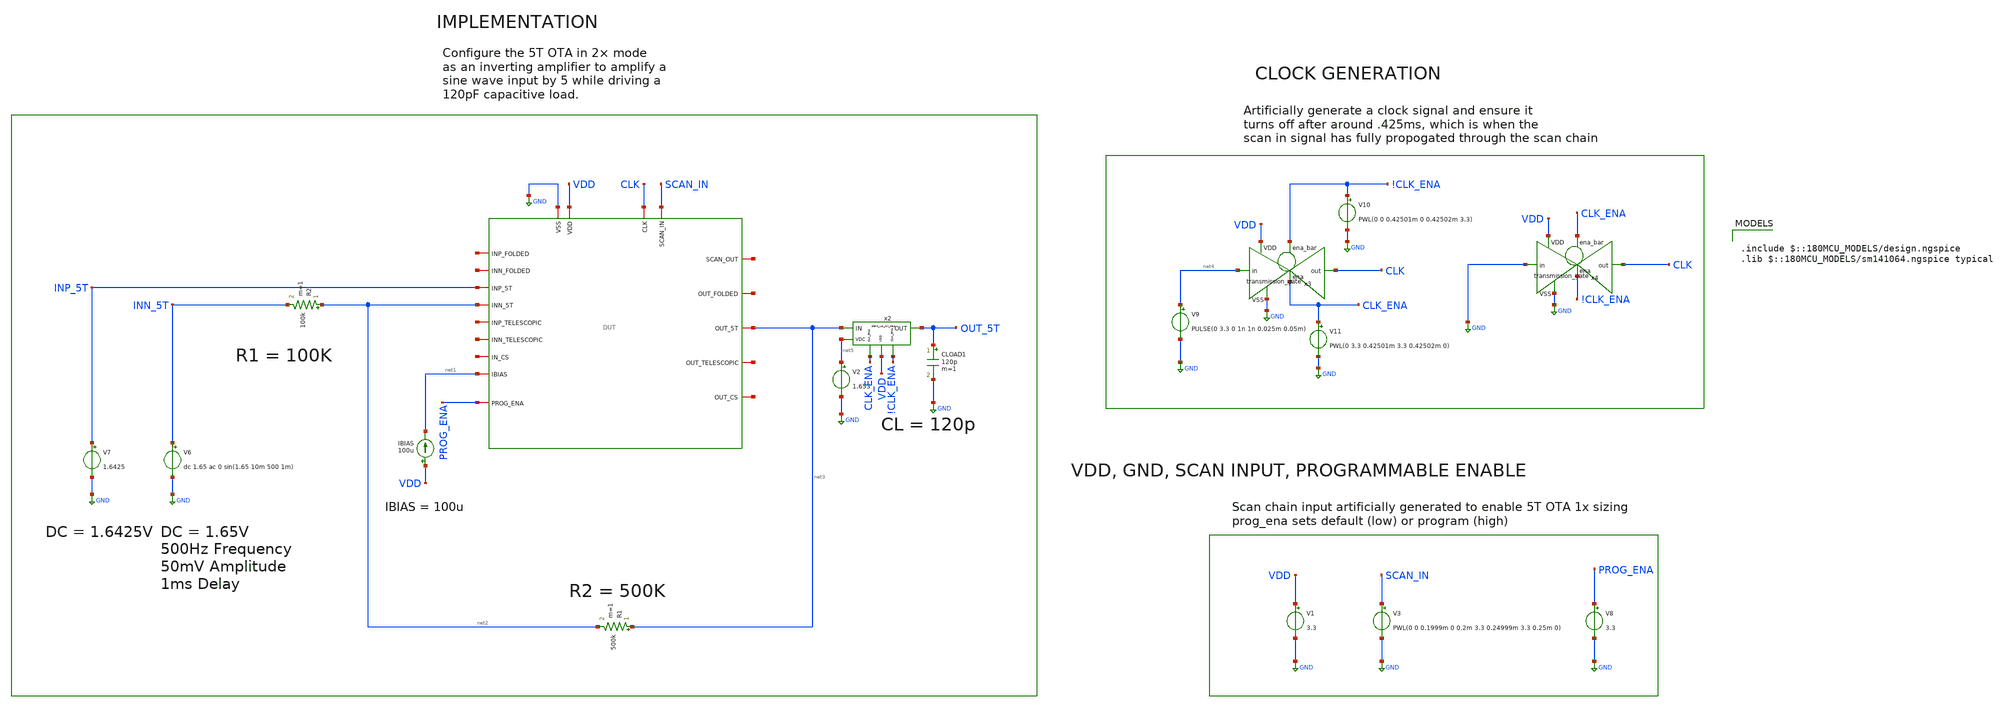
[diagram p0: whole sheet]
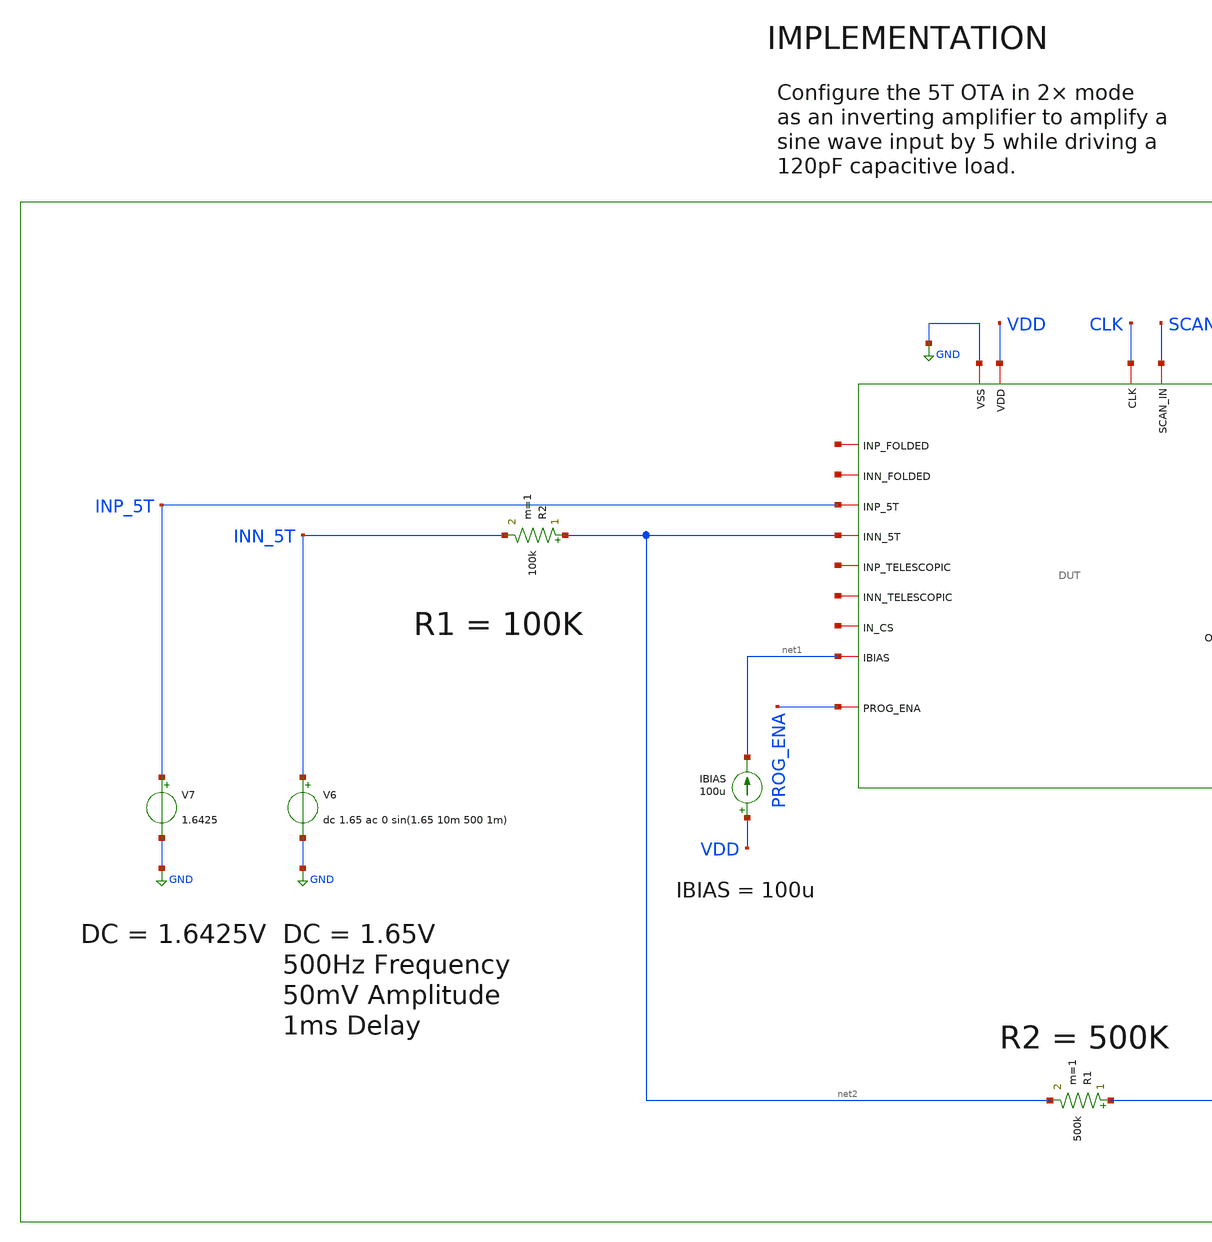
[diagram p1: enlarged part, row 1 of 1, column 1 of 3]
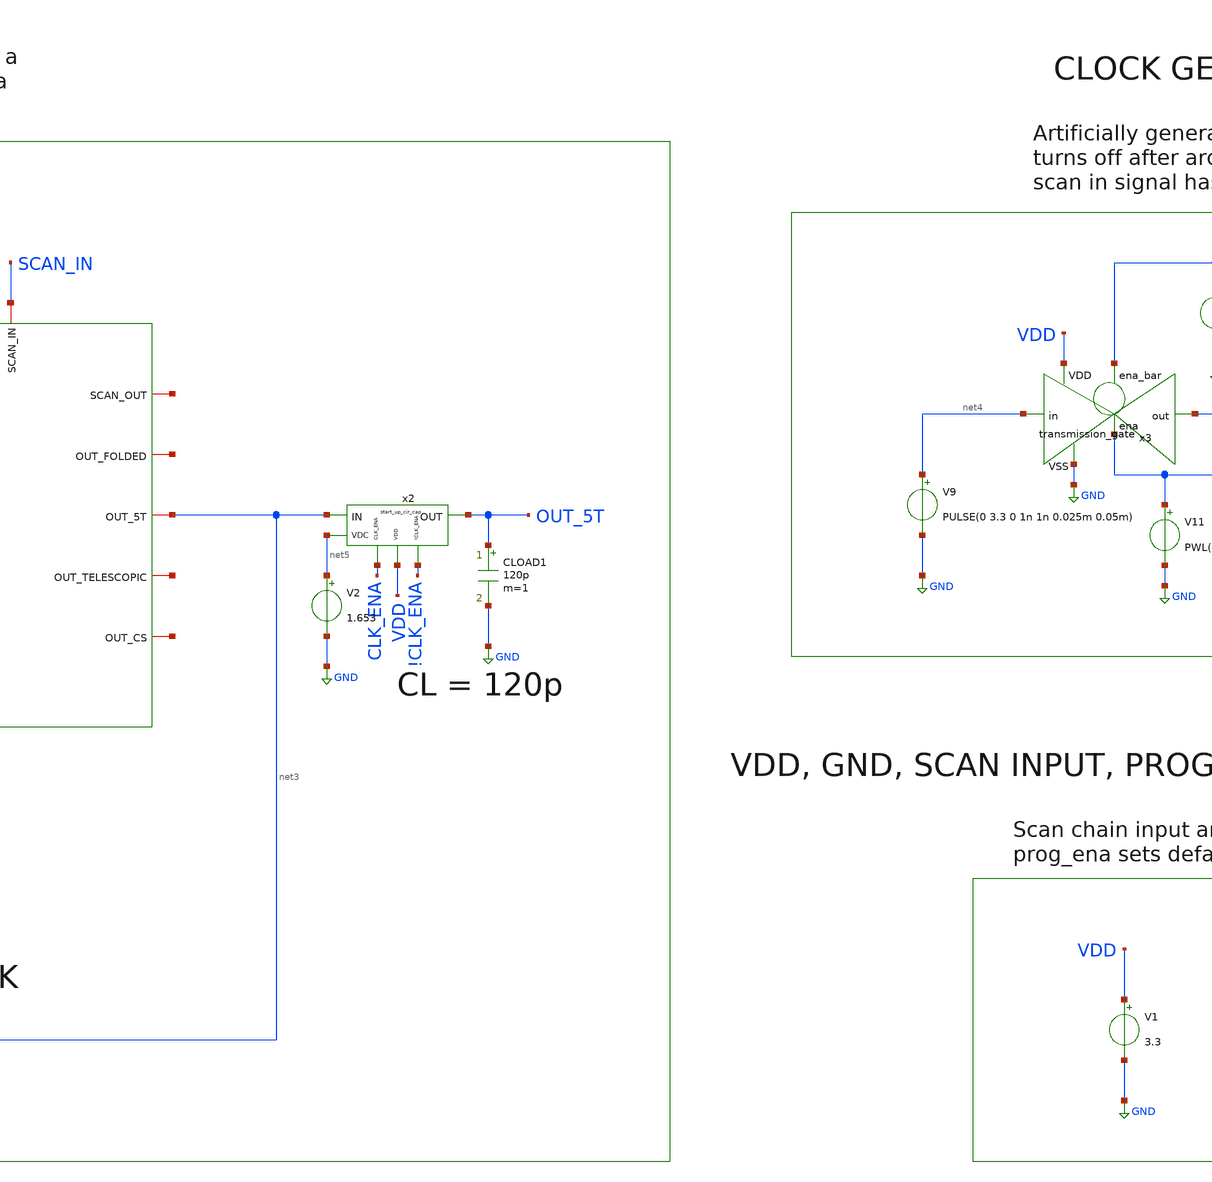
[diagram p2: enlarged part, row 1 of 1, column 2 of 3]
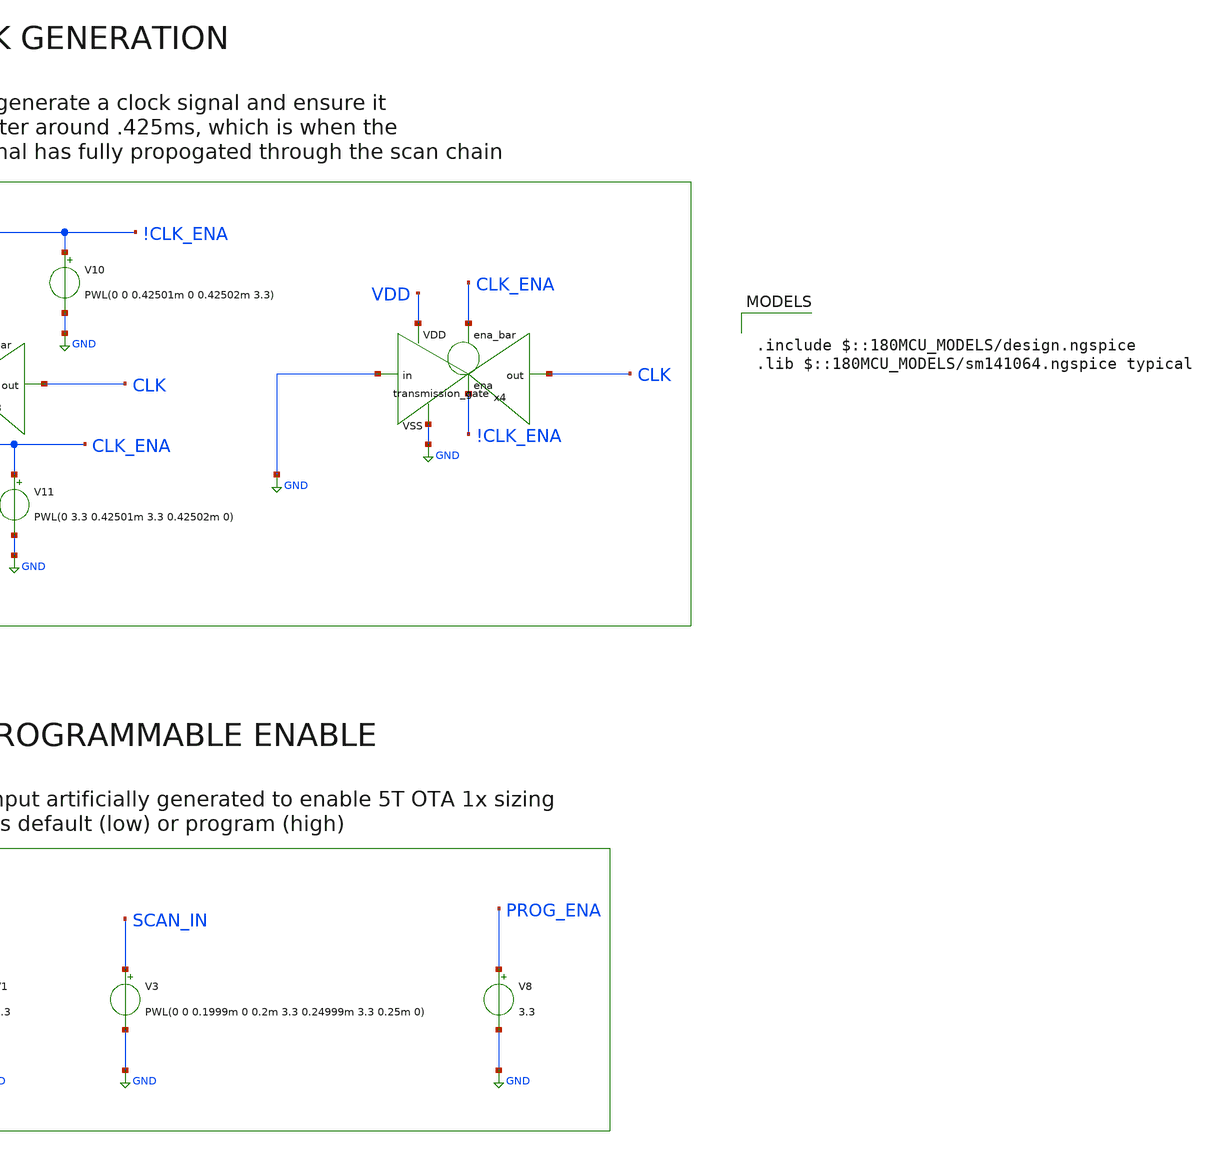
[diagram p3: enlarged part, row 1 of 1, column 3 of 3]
** sch_path: designs/libs/pex/5t/inverting_amplifier/with_start_cir/with_cap/default_inverting_5t.sch
**.subckt default_inverting_5t
V3 SCAN_IN GND PWL(0 0 0.1999m 0 0.2m 3.3 0.24999m 3.3 0.25m 0)
V1 VDD GND 3.3
IBIAS VDD net1 100u
V7 INP_5T GND 1.6425
R2 net2 INN_5T 100k m=1
V6 INN_5T GND dc 1.65 ac 0 sin(1.65 10m 500 1m)
R1 net3 net2 500k m=1
V8 PROG_ENA GND 3.3
V9 net4 GND PULSE(0 3.3 0 1n 1n 0.025m 0.05m)
x3 !CLK_ENA VDD CLK net4 GND CLK_ENA transmission_gate
V10 !CLK_ENA GND PWL(0 0 0.42501m 0 0.42502m 3.3)
V11 CLK_ENA GND PWL(0 3.3 0.42501m 3.3 0.42502m 0)
x4 CLK_ENA VDD CLK GND GND !CLK_ENA transmission_gate
x1 CLK net6 SCAN_IN GND VDD net7 net8 net3 net1 net9 INP_5T net2 net10 net11 net12 net13 net14
+ PROG_ENA DUT
CLOAD1 OUT_5T GND 120p m=1
V2 net5 GND 1.653
x2 CLK_ENA VDD !CLK_ENA net3 OUT_5T net5 start_up_cir_cap
**** begin user architecture code

.include $::180MCU_MODELS/design.ngspice
.lib $::180MCU_MODELS/sm141064.ngspice typical



.include /foss/designs/libs/pex/DUT.spice
.control
tran 1u 5m

set color0 = white
set color1 = black
plot v(out_5T) v(inn_5T)
wrdata /foss/designs/libs/pex/5t/inverting_amplifier/with_start_cir/with_cap/default.csv v(out_5T)
+ v(inn_5T)

meas tran vout_pp pp v(out_5T) from=2m to=5m
meas tran vin_pp pp v(inn_5T) from=2m to=5m
let gain = vout_pp / vin_pp
print gain

meas tran vout_dc avg v(out_5T) from=2m to=5m
meas tran vin_dc avg v(inn_5T) from=2m to=5m
let dc_offset = vout_dc - vin_dc
let input_offset = dc_offset / 6
print vout_dc vin_dc dc_offset input_offset

let ideal_gain = 5
let gain_error_pct = (ideal_gain - gain) / ideal_gain * 100
print gain_error_pct

meas tran idd avg i(v1) from=2m to=5m
let power = abs(idd) * 3.3
print idd power
.endc


**** end user architecture code
**.ends

* expanding   symbol:  libs/core_digital/schem/transmission_gate.sym # of pins=6
** sym_path: designs/libs/core_digital/schem/transmission_gate.sym
** sch_path: designs/libs/core_digital/schem/transmission_gate.sch
.subckt transmission_gate ena_bar VDD out in VSS ena
*.ipin in
*.ipin ena_bar
*.ipin ena
*.ipin VSS
*.ipin VDD
*.opin out
XM1 in ena_bar out VDD pfet_03v3 L=0.28u W=0.22u nf=1 ad='int((nf+1)/2) * W/nf * 0.18u' as='int((nf+2)/2) * W/nf * 0.18u'
+ pd='2*int((nf+1)/2) * (W/nf + 0.18u)' ps='2*int((nf+2)/2) * (W/nf + 0.18u)' nrd='0.18u / W' nrs='0.18u / W'
+ sa=0 sb=0 sd=0 m=1
XM2 in ena out VSS nfet_03v3 L=0.28u W=0.22u nf=1 ad='int((nf+1)/2) * W/nf * 0.18u' as='int((nf+2)/2) * W/nf * 0.18u'
+ pd='2*int((nf+1)/2) * (W/nf + 0.18u)' ps='2*int((nf+2)/2) * (W/nf + 0.18u)' nrd='0.18u / W' nrs='0.18u / W'
+ sa=0 sb=0 sd=0 m=1
.ends


* expanding   symbol:  libs/core_amps/start_up_cir/start_up_cir_cap.sym # of pins=6
** sym_path: designs/libs/core_amps/start_up_cir/start_up_cir_cap.sym
** sch_path: designs/libs/core_amps/start_up_cir/start_up_cir_cap.sch
.subckt start_up_cir_cap CLK_ENA VDD !CLK_ENA IN OUT VDC
*.ipin IN
*.opin OUT
*.ipin VDC
*.ipin VDD
*.ipin CLK_ENA
*.ipin !CLK_ENA
x2 !CLK_ENA VDD OUT VDC GND CLK_ENA transmission_gate
x5 CLK_ENA VDD OUT IN GND !CLK_ENA transmission_gate
C OUT GND 1n m=1
.ends

.GLOBAL GND
.end
